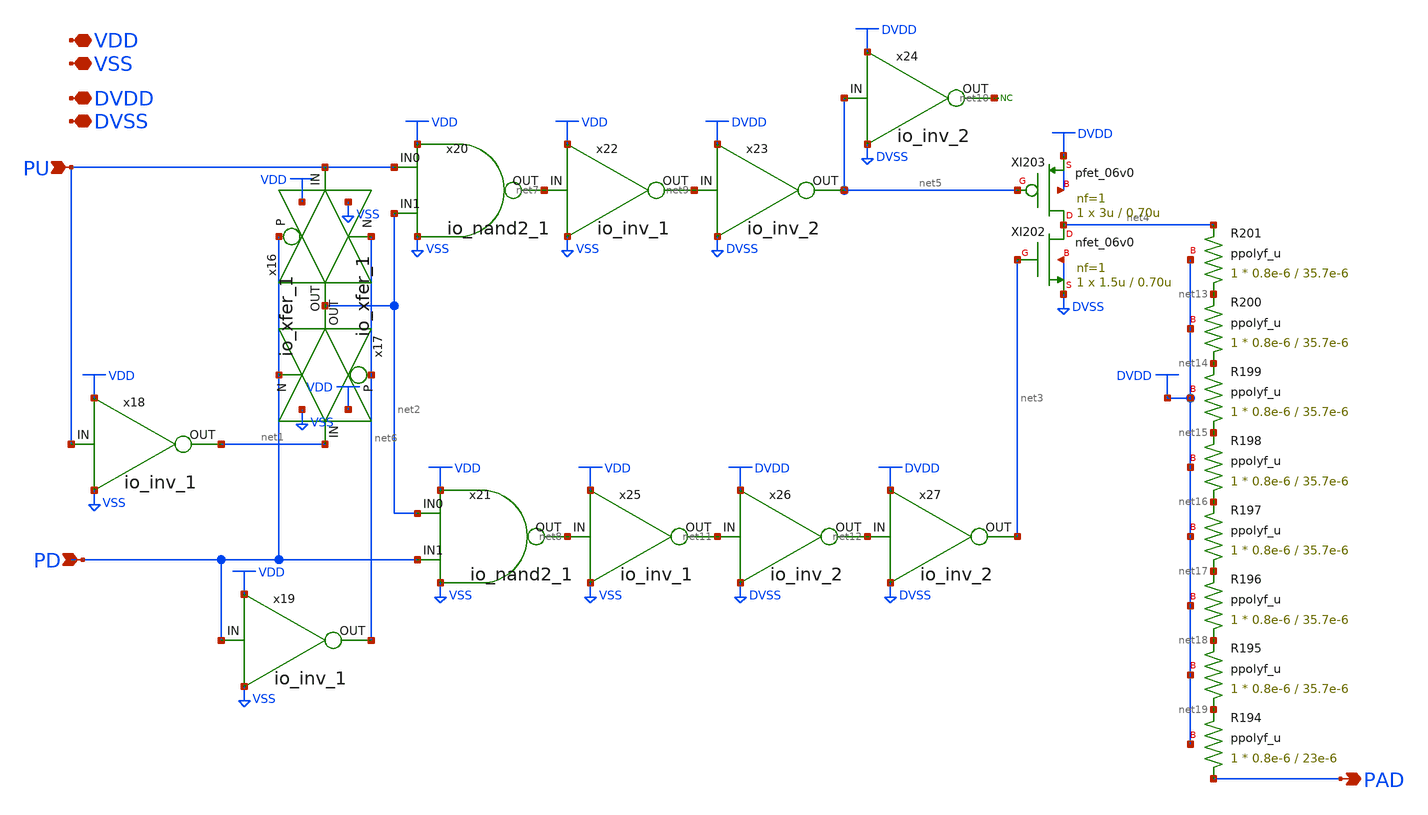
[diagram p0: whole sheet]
** sch_path: io_pupd.sch
**.subckt io_pupd PU PD PAD VDD VSS DVDD DVSS
*.ipin PU
*.ipin PD
*.opin PAD
*.iopin VDD
*.iopin VSS
*.iopin DVDD
*.iopin DVSS
x16 PU net2 PD net6 VDD VSS io_xfer_1
x17 net1 net2 net6 PD VDD VSS io_xfer_1
x18 PU net1 VDD VSS io_inv_1
x19 PD net6 VDD VSS io_inv_1
x20 PU net7 net2 VDD VSS io_nand2_1
x21 net2 net8 PD VDD VSS io_nand2_1
x22 net7 net9 VDD VSS io_inv_1
x23 net9 net5 DVDD DVSS io_inv_2
x24 net5 net10 DVDD DVSS io_inv_2
x25 net8 net11 VDD VSS io_inv_1
x26 net11 net12 DVDD DVSS io_inv_2
x27 net12 net3 DVDD DVSS io_inv_2
XI202 net4 net3 DVSS DVSS nfet_06v0 L=0.70u W=1.5u nf=1 ad='int((nf+1)/2) * W/nf * 0.18u' as='int((nf+2)/2) * W/nf * 0.18u'
+ pd='2*int((nf+1)/2) * (W/nf + 0.18u)' ps='2*int((nf+2)/2) * (W/nf + 0.18u)' nrd='0.18u / W' nrs='0.18u / W'
+ sa=0 sb=0 sd=0 m=1
XI203 net4 net5 DVDD DVDD pfet_06v0 L=0.70u W=3u nf=1 ad='int((nf+1)/2) * W/nf * 0.18u' as='int((nf+2)/2) * W/nf * 0.18u'
+ pd='2*int((nf+1)/2) * (W/nf + 0.18u)' ps='2*int((nf+2)/2) * (W/nf + 0.18u)' nrd='0.18u / W' nrs='0.18u / W'
+ sa=0 sb=0 sd=0 m=1
XR201 net13 net4 DVDD ppolyf_u r_width=0.8e-6 r_length=35.7e-6 m=1
XR200 net14 net13 DVDD ppolyf_u r_width=0.8e-6 r_length=35.7e-6 m=1
XR199 net15 net14 DVDD ppolyf_u r_width=0.8e-6 r_length=35.7e-6 m=1
XR198 net16 net15 DVDD ppolyf_u r_width=0.8e-6 r_length=35.7e-6 m=1
XR197 net17 net16 DVDD ppolyf_u r_width=0.8e-6 r_length=35.7e-6 m=1
XR196 net18 net17 DVDD ppolyf_u r_width=0.8e-6 r_length=35.7e-6 m=1
XR195 net19 net18 DVDD ppolyf_u r_width=0.8e-6 r_length=35.7e-6 m=1
XR194 PAD net19 DVDD ppolyf_u r_width=0.8e-6 r_length=23e-6 m=1
* noconn #net10
**.ends

* expanding   symbol:  io_xfer_1.sym # of pins=6
** sym_path: io_xfer_1.sym
** sch_path: io_xfer_1.sch
.subckt io_xfer_1 IN OUT P N VDD VSS
*.opin OUT
*.ipin IN
*.ipin N
*.ipin P
*.iopin VDD
*.iopin VSS
XM1 OUT P IN VDD pfet_06v0 L=0.70u W=3u nf=1 ad='int((nf+1)/2) * W/nf * 0.18u' as='int((nf+2)/2) * W/nf * 0.18u'
+ pd='2*int((nf+1)/2) * (W/nf + 0.18u)' ps='2*int((nf+2)/2) * (W/nf + 0.18u)' nrd='0.18u / W' nrs='0.18u / W'
+ sa=0 sb=0 sd=0 m=1
XM3 OUT N IN VSS nfet_06v0 L=0.70u W=1.5u nf=1 ad='int((nf+1)/2) * W/nf * 0.18u' as='int((nf+2)/2) * W/nf * 0.18u'
+ pd='2*int((nf+1)/2) * (W/nf + 0.18u)' ps='2*int((nf+2)/2) * (W/nf + 0.18u)' nrd='0.18u / W' nrs='0.18u / W'
+ sa=0 sb=0 sd=0 m=1
.ends


* expanding   symbol:  io_nand2_1.sym # of pins=5
** sym_path: io_nand2_1.sym
** sch_path: io_nand2_1.sch
.subckt io_nand2_1 IN0 OUT IN1 VDD VSS
*.opin OUT
*.ipin IN0
*.ipin IN1
*.iopin VDD
*.iopin VSS
XM1 OUT IN1 VDD VDD pfet_06v0 L=0.70u W=3u nf=1 ad='int((nf+1)/2) * W/nf * 0.18u' as='int((nf+2)/2) * W/nf * 0.18u'
+ pd='2*int((nf+1)/2) * (W/nf + 0.18u)' ps='2*int((nf+2)/2) * (W/nf + 0.18u)' nrd='0.18u / W' nrs='0.18u / W'
+ sa=0 sb=0 sd=0 m=1
XM2 net1 IN0 VSS VSS nfet_06v0 L=0.70u W=3u nf=1 ad='int((nf+1)/2) * W/nf * 0.18u' as='int((nf+2)/2) * W/nf * 0.18u'
+ pd='2*int((nf+1)/2) * (W/nf + 0.18u)' ps='2*int((nf+2)/2) * (W/nf + 0.18u)' nrd='0.18u / W' nrs='0.18u / W'
+ sa=0 sb=0 sd=0 m=1
XM3 OUT IN1 net1 VSS nfet_06v0 L=0.70u W=3u nf=1 ad='int((nf+1)/2) * W/nf * 0.18u' as='int((nf+2)/2) * W/nf * 0.18u'
+ pd='2*int((nf+1)/2) * (W/nf + 0.18u)' ps='2*int((nf+2)/2) * (W/nf + 0.18u)' nrd='0.18u / W' nrs='0.18u / W'
+ sa=0 sb=0 sd=0 m=1
XM4 OUT IN0 VDD VDD pfet_06v0 L=0.70u W=3u nf=1 ad='int((nf+1)/2) * W/nf * 0.18u' as='int((nf+2)/2) * W/nf * 0.18u'
+ pd='2*int((nf+1)/2) * (W/nf + 0.18u)' ps='2*int((nf+2)/2) * (W/nf + 0.18u)' nrd='0.18u / W' nrs='0.18u / W'
+ sa=0 sb=0 sd=0 m=1
.ends


* expanding   symbol:  io_inv_2.sym # of pins=4
** sym_path: io_inv_2.sym
** sch_path: io_inv_2.sch
.subckt io_inv_2 IN OUT VDD VSS
*.opin OUT
*.ipin IN
*.iopin VDD
*.iopin VSS
XM1 OUT IN VDD VDD pfet_06v0 L=0.70u W=6u nf=1 ad='int((nf+1)/2) * W/nf * 0.18u' as='int((nf+2)/2) * W/nf * 0.18u'
+ pd='2*int((nf+1)/2) * (W/nf + 0.18u)' ps='2*int((nf+2)/2) * (W/nf + 0.18u)' nrd='0.18u / W' nrs='0.18u / W'
+ sa=0 sb=0 sd=0 m=1
XM3 OUT IN VSS VSS nfet_06v0 L=0.70u W=3u nf=1 ad='int((nf+1)/2) * W/nf * 0.18u' as='int((nf+2)/2) * W/nf * 0.18u'
+ pd='2*int((nf+1)/2) * (W/nf + 0.18u)' ps='2*int((nf+2)/2) * (W/nf + 0.18u)' nrd='0.18u / W' nrs='0.18u / W'
+ sa=0 sb=0 sd=0 m=1
.ends

.GLOBAL DVDD
.GLOBAL VDD
.end
